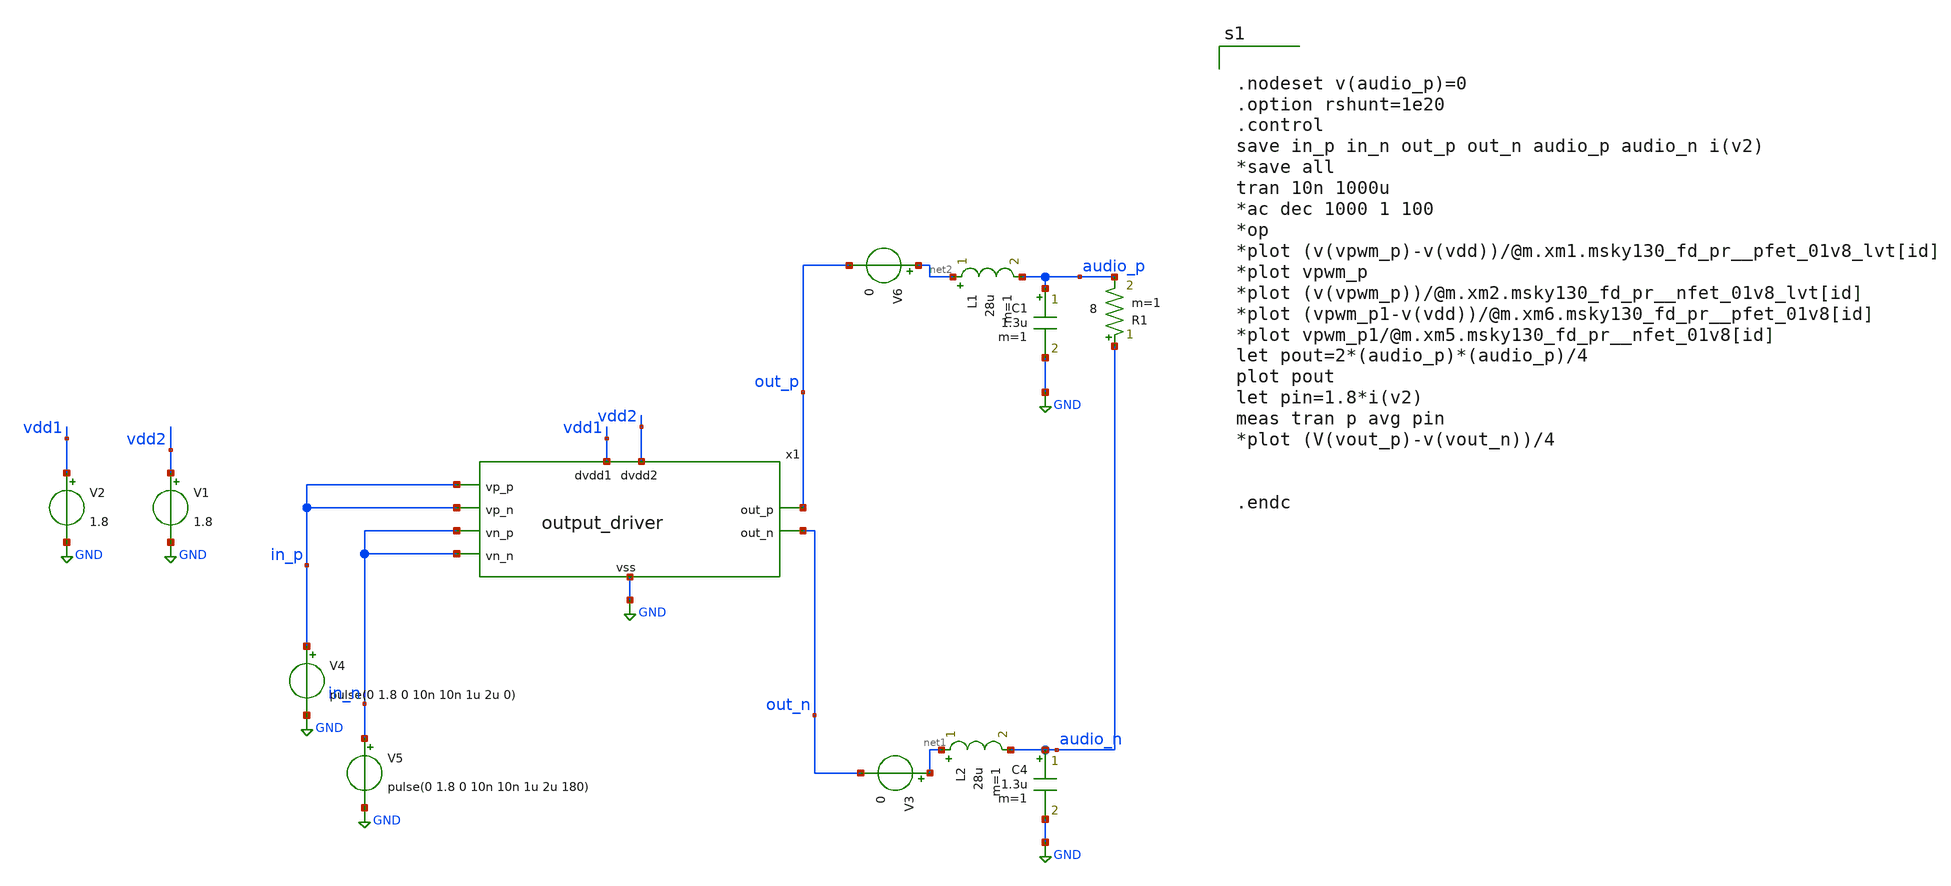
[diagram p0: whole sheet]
** sch_path: xschem/src/output_driver/output_driver_tb.sch
**.subckt output_driver_tb
V2 vdd1 GND 1.8
V4 in_p GND pulse(0 1.8 0 10n 10n 1u 2u 0)
V5 in_n GND pulse(0 1.8 0 10n 10n 1u 2u 180)
L2 net1 audio_n 28u m=1
C4 audio_n GND 1.3u m=1
R1 audio_n audio_p 8 m=1
V1 vdd2 GND 1.8
V3 net1 out_n 0
L1 net2 audio_p 28u m=1
C1 audio_p GND 1.3u m=1
V6 net2 out_p 0
x1 vdd1 in_p out_p GND in_p vdd2 in_n out_n in_n output_driver
**** begin user architecture code


.nodeset v(audio_p)=0
.option rshunt=1e20
.control
save in_p in_n out_p out_n audio_p audio_n i(v2)
*save all
tran 10n 1000u
*ac dec 1000 1 100
*op
*plot (v(vpwm_p)-v(vdd))/@m.xm1.msky130_fd_pr__pfet_01v8_lvt[id]
*plot vpwm_p
*plot (v(vpwm_p))/@m.xm2.msky130_fd_pr__nfet_01v8_lvt[id]
*plot (vpwm_p1-v(vdd))/@m.xm6.msky130_fd_pr__pfet_01v8[id]
*plot vpwm_p1/@m.xm5.msky130_fd_pr__nfet_01v8[id]
let pout=2*(audio_p)*(audio_p)/4
plot pout
let pin=1.8*i(v2)
meas tran p avg pin
*plot (V(vout_p)-v(vout_n))/4


.endc






.include /home/eda/pdk/skywater-pdk/libraries/sky130_fd_pr_ngspice/latest/models/corners/tt.spice
.include /home/eda/magic/class_d_audio_amplifier/OTA/OTA_int_post.spice
.include /home/eda/magic/class_d_audio_amplifier/OTA/OTA_post.spice
.include /home/eda/magic/class_d_audio_amplifier/S_to_D/S_to_D_post.spice
.include /home/eda/magic/class_d_audio_amplifier/triang/triangle_post.spice
.include /home/eda/magic/class_d_audio_amplifier/output_driver/output_driver_post.spice
.include /home/eda/magic/class_d_audio_amplifier/output_driver/half_driver_post.spice
* Resistor$::SKYWATER_MODELS/Capacitor
.include $::SKYWATER_MODELS/models/r+c/res_typical__cap_typical.spice
.include $::SKYWATER_MODELS/models/r+c/res_typical__cap_typical__lin.spice
* Special cells
.include $::SKYWATER_MODELS/models/corners/tt/specialized_cells.spice


**** end user architecture code
**.ends

* expanding   symbol:  src/output_driver/output_driver.sym # of pins=9
** sym_path: xschem/src/output_driver/output_driver.sym
** sch_path: xschem/src/output_driver/output_driver.sch
.subckt output_driver dvdd1 vp_p out_p vss vp_n dvdd2 vn_p out_n vn_n
*.ipin vp_p
*.ipin vp_n
*.ipin vn_p
*.ipin vn_n
*.opin out_p
*.opin out_n
*.iopin dvdd1
*.iopin vss
*.iopin dvdd2
x1 dvdd1 vss vp_p out_p vp_n half_driver
x2 dvdd2 vss vn_p out_n vn_n half_driver
.ends


* expanding   symbol:  src/output_driver/half_driver.sym # of pins=5
** sym_path: xschem/src/output_driver/half_driver.sym
** sch_path: xschem/src/output_driver/half_driver.sch
.subckt half_driver vdd vss vp_p out_p vp_n
*.ipin vp_p
*.ipin vp_n
*.opin out_p
*.iopin vdd
*.iopin vss
XM1 out_p vp_p vdd vdd sky130_fd_pr__pfet_01v8 L=0.15 W=12000 nf=200 ad='int((nf+1)/2) * W/nf * 0.29'
+ as='int((nf+2)/2) * W/nf * 0.29' pd='2*int((nf+1)/2) * (W/nf + 0.29)' ps='2*int((nf+2)/2) * (W/nf + 0.29)'
+ nrd='0.29 / W' nrs='0.29 / W' sa=0 sb=0 sd=0 mult=1 m=1
XM2 out_p vp_n vss vss sky130_fd_pr__nfet_01v8 L=0.15 W=2400 nf=100 ad='int((nf+1)/2) * W/nf * 0.29'
+ as='int((nf+2)/2) * W/nf * 0.29' pd='2*int((nf+1)/2) * (W/nf + 0.29)' ps='2*int((nf+2)/2) * (W/nf + 0.29)'
+ nrd='0.29 / W' nrs='0.29 / W' sa=0 sb=0 sd=0 mult=1 m=1
.ends

.GLOBAL GND
.end
